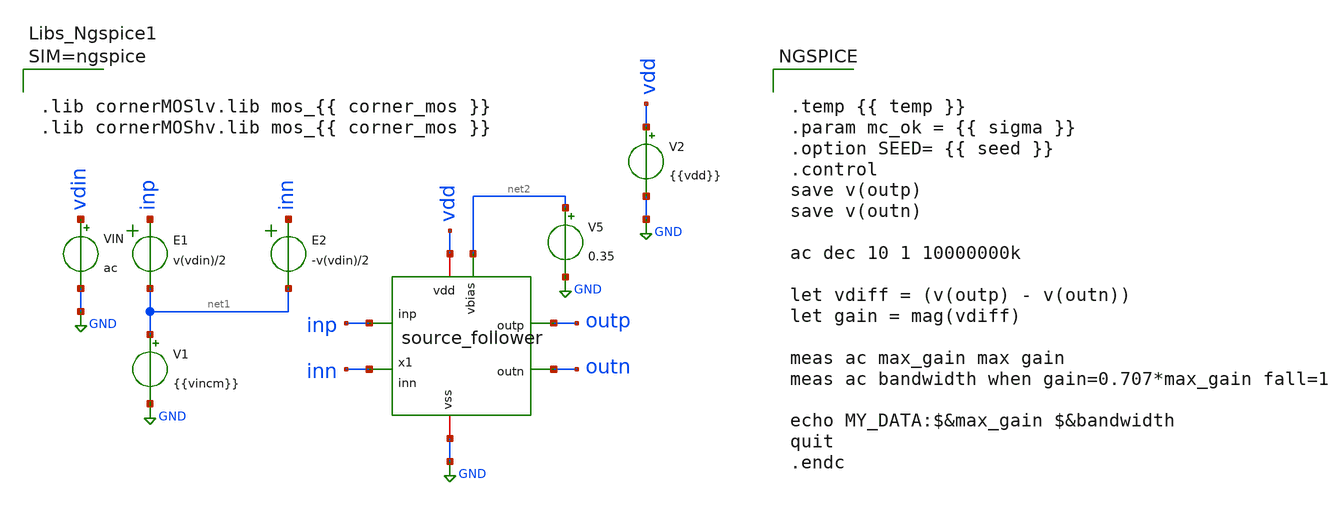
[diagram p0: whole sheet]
** sch_path: examples/source_follower/tb/tb_sf_gain.sch
**.subckt tb_sf_gain
E1 inp net1 VOL=' v(vdin)/2 '
E2 inn net1 VOL=' -v(vdin)/2 '
V1 net1 GND {{vincm}}
.save i(v1)
V2 vdd GND {{vdd}}
V5 net2 GND 0.35
.save i(v5)
VIN vdin GND ac
.save i(vin)
x1 vdd inn inp outp outn net2 GND source_follower
**** begin user architecture code


.temp {{ temp }}
.param mc_ok = {{ sigma }}
.option SEED= {{ seed }}
.control
save v(outp)
save v(outn)

ac dec 10 1 10000000k

let vdiff = (v(outp) - v(outn))
let gain = mag(vdiff)

meas ac max_gain max gain
meas ac bandwidth when gain=0.707*max_gain fall=1

echo MY_DATA:$&max_gain $&bandwidth
quit
.endc





.lib cornerMOSlv.lib mos_{{ corner_mos }}
.lib cornerMOShv.lib mos_{{ corner_mos }}



**** end user architecture code
**.ends

* expanding   symbol:  chipify/examples/source_follower/sch/source_follower.sym # of pins=7
** sym_path: examples/source_follower/sch/source_follower.sym
** sch_path: examples/source_follower/sch/source_follower.sch
.subckt source_follower vdd inn inp outp outn vbias vss
*.ipin vbias
*.iopin vdd
*.opin outp
*.iopin vss
*.opin outn
*.ipin inp
*.ipin inn
XM1 outp vbias vss vss sg13_lv_nmos w=100u l=2u ng=20 m=1 mm_ok=1
XM2 vdd inp outp vss sg13_lv_nmos w=200u l=0.13u ng=20 m=1 mm_ok=1
XM3 outn vbias vss vss sg13_lv_nmos w=100u l=2u ng=20 m=1 mm_ok=1
XM4 vdd inn outn vss sg13_lv_nmos w=200u l=0.13u ng=20 m=1 mm_ok=1
.ends

.GLOBAL GND
.end
